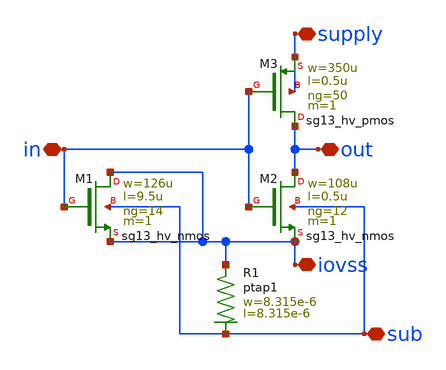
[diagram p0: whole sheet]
** sch_path: MSPHY6034-main/schematic/xschem/openpdk-libraries/ihp-sg13g2/sg13g2_io/xschem/sg13g2_RCClampInverter.sch
**.subckt sg13g2_RCClampInverter supply iovss out in sub
*.iopin supply
*.iopin iovss
*.iopin out
*.iopin in
*.iopin sub
XR1 iovss sub ptap1 R=9.57 w=8.315e-6 l=8.315e-6
XM1 iovss in iovss sub sg13_hv_nmos w=126u l=9.5u ng=14 m=1 mm_ok=1
XM2 out in iovss sub sg13_hv_nmos w=108u l=0.5u ng=12 m=1 mm_ok=1
XM3 out in supply supply sg13_hv_pmos w=350u l=0.5u ng=50 m=1 mm_ok=1
**.ends
.end
